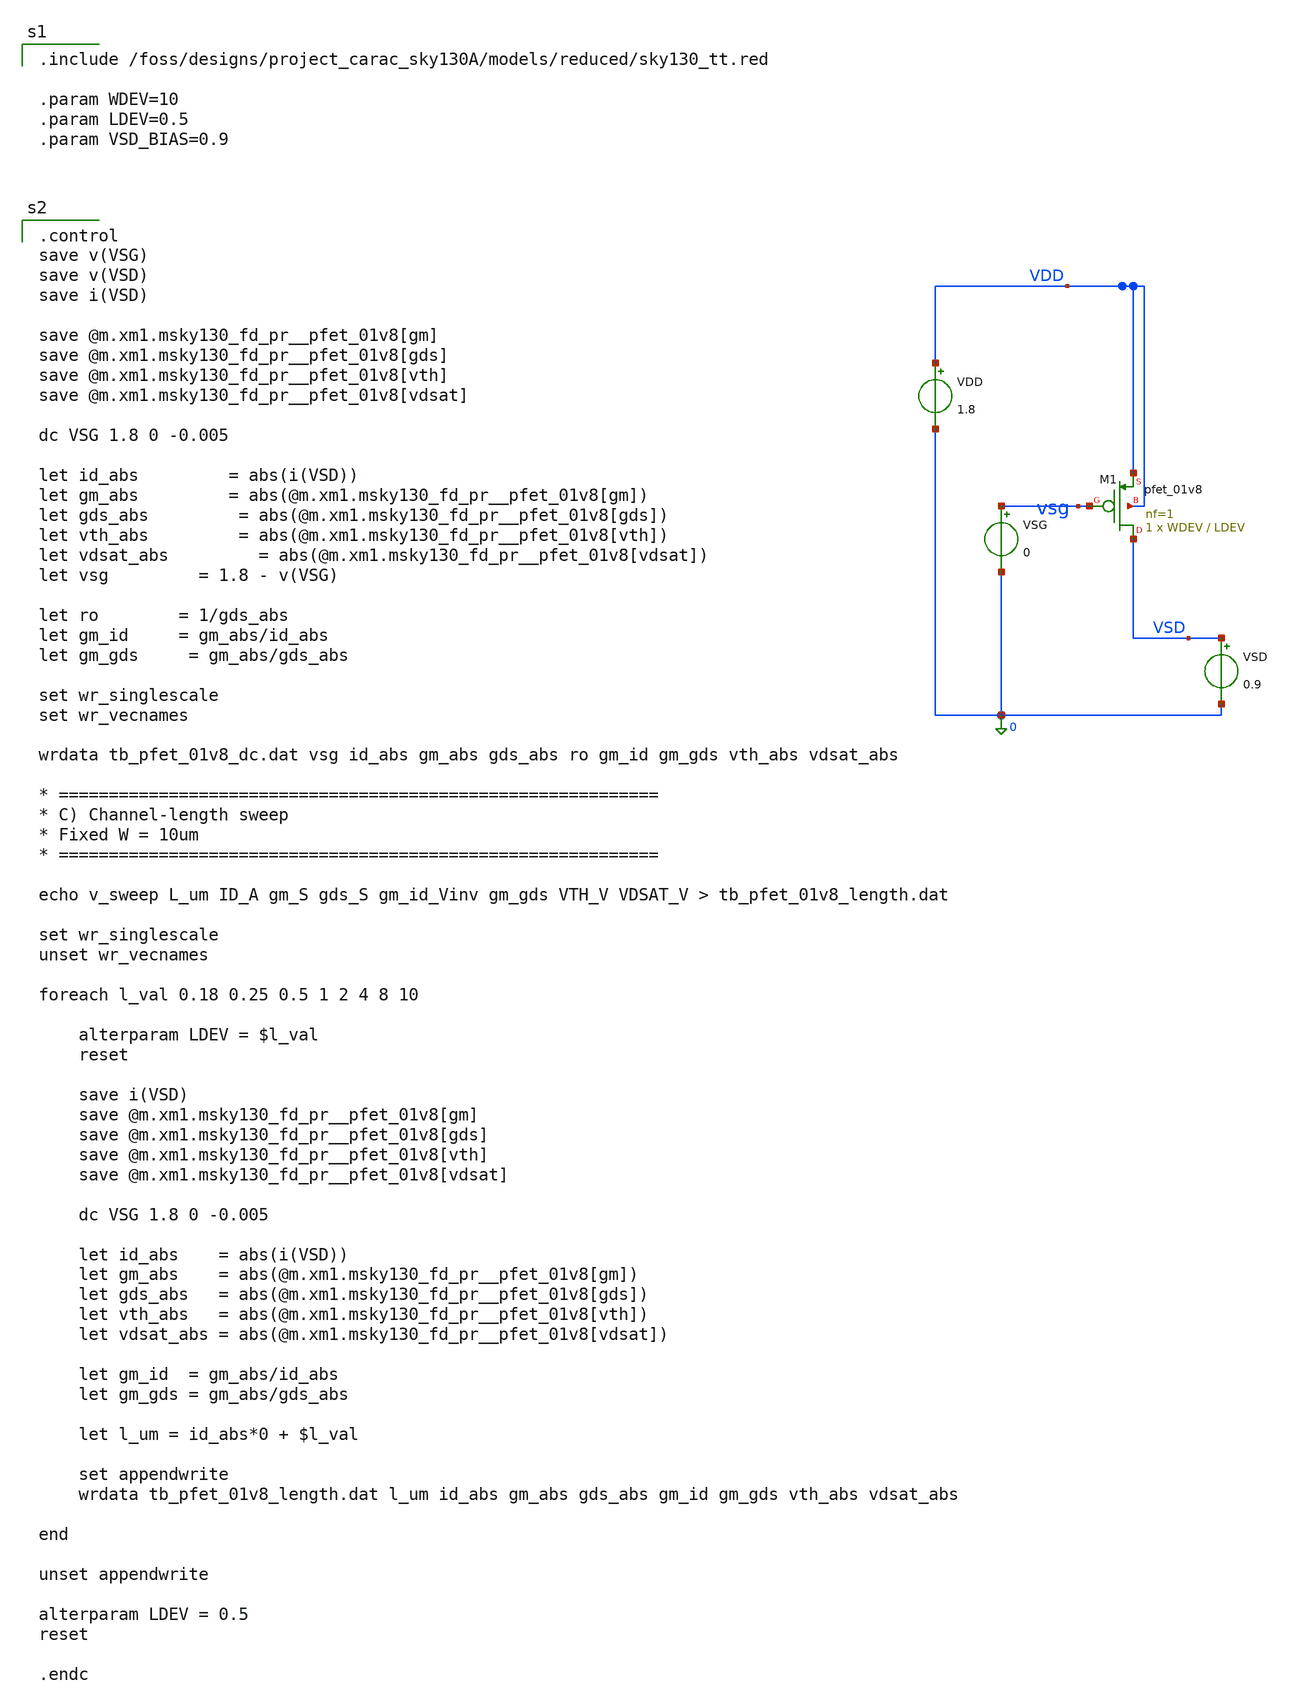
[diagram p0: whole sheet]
** sch_path: dfii/project_carac_sky130A_sim/tb_pfet_01v8_dc.sch
* Copyright 2021 Stefan Frederik Schippers
* Licensed under the Apache License, Version 2.0 (the "License");
* you may not use this file except in compliance with the License.
* You may obtain a copy of the License at
* https://www.apache.org/licenses/LICENSE-2.0
* Unless required by applicable law or agreed to in writing, software
* distributed under the License is distributed on an "AS IS" BASIS,
* WITHOUT WARRANTIES OR CONDITIONS OF ANY KIND, either express or implied.
* See the License for the specific language governing permissions and
* limitations under the License.

.include /foss/designs/project_carac_sky130A/models/reduced/sky130_tt.red

.param WDEV=10
.param LDEV=0.5
.param VSD_BIAS=0.9



**.subckt tb_pfet_01v8_dc
VSG vsg 0 0
VSD VSD 0 0.9
.save i(vsd)
XM1 VSD vsg VDD VDD sky130_fd_pr__pfet_01v8 L=LDEV W=WDEV nf=1 ad='int((1 + 1)/2) * WDEV / 1 * 0.29'
+ as='int((1 + 2)/2) * WDEV / 1 * 0.29' pd='2*int((1 + 1)/2) * (WDEV / 1 + 0.29)' ps='2*int((1 + 2)/2) * (WDEV / 1 + 0.29)'
+ nrd='0.29 / WDEV ' nrs='0.29 / WDEV ' sa=0 sb=0 sd=0 mult=1 m=1
VDD VDD 0 1.8
**.ends
**** begin user architecture code

.control
save v(VSG)
save v(VSD)
save i(VSD)

save @m.xm1.msky130_fd_pr__pfet_01v8[gm]
save @m.xm1.msky130_fd_pr__pfet_01v8[gds]
save @m.xm1.msky130_fd_pr__pfet_01v8[vth]
save @m.xm1.msky130_fd_pr__pfet_01v8[vdsat]

dc VSG 1.8 0 -0.005

let id_abs 		= abs(i(VSD))
let gm_abs 		= abs(@m.xm1.msky130_fd_pr__pfet_01v8[gm])
let gds_abs 		= abs(@m.xm1.msky130_fd_pr__pfet_01v8[gds])
let vth_abs 		= abs(@m.xm1.msky130_fd_pr__pfet_01v8[vth])
let vdsat_abs 		= abs(@m.xm1.msky130_fd_pr__pfet_01v8[vdsat])
let vsg 		= 1.8 - v(VSG)

let ro		= 1/gds_abs
let gm_id 	= gm_abs/id_abs
let gm_gds 	= gm_abs/gds_abs

set wr_singlescale
set wr_vecnames

wrdata tb_pfet_01v8_dc.dat vsg id_abs gm_abs gds_abs ro gm_id gm_gds vth_abs vdsat_abs

* ============================================================
* C) Channel-length sweep
* Fixed W = 10um
* ============================================================

echo v_sweep L_um ID_A gm_S gds_S gm_id_Vinv gm_gds VTH_V VDSAT_V > tb_pfet_01v8_length.dat

set wr_singlescale
unset wr_vecnames

foreach l_val 0.18 0.25 0.5 1 2 4 8 10

    alterparam LDEV = $l_val
    reset

    save i(VSD)
    save @m.xm1.msky130_fd_pr__pfet_01v8[gm]
    save @m.xm1.msky130_fd_pr__pfet_01v8[gds]
    save @m.xm1.msky130_fd_pr__pfet_01v8[vth]
    save @m.xm1.msky130_fd_pr__pfet_01v8[vdsat]

    dc VSG 1.8 0 -0.005

    let id_abs    = abs(i(VSD))
    let gm_abs    = abs(@m.xm1.msky130_fd_pr__pfet_01v8[gm])
    let gds_abs   = abs(@m.xm1.msky130_fd_pr__pfet_01v8[gds])
    let vth_abs   = abs(@m.xm1.msky130_fd_pr__pfet_01v8[vth])
    let vdsat_abs = abs(@m.xm1.msky130_fd_pr__pfet_01v8[vdsat])

    let gm_id  = gm_abs/id_abs
    let gm_gds = gm_abs/gds_abs

    let l_um = id_abs*0 + $l_val

    set appendwrite
    wrdata tb_pfet_01v8_length.dat l_um id_abs gm_abs gds_abs gm_id gm_gds vth_abs vdsat_abs

end

unset appendwrite

alterparam LDEV = 0.5
reset

.endc

**** end user architecture code
.end
